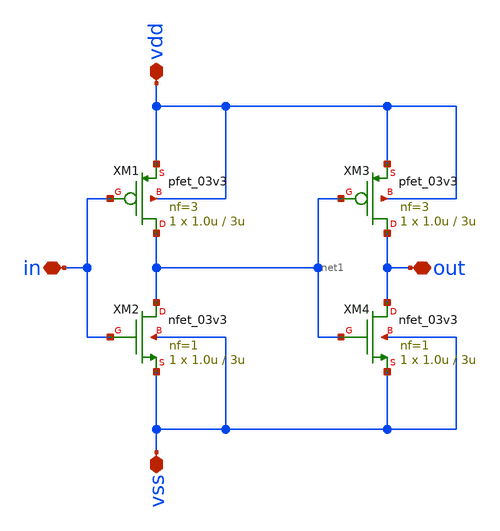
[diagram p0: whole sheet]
** sch_path: designs/libs/core_analog/asc_delay_1ns/asc_delay_1ns.sch
**.subckt asc_delay_1ns in vss vdd out
*.iopin in
*.iopin vss
*.iopin vdd
*.iopin out
XM1 net1 in vdd vdd pfet_03v3 L=3u W=1.0u nf=3 ad='int((nf+1)/2) * W/nf * 0.18u' as='int((nf+2)/2) * W/nf * 0.18u'
+ pd='2*int((nf+1)/2) * (W/nf + 0.18u)' ps='2*int((nf+2)/2) * (W/nf + 0.18u)' nrd='0.18u / W' nrs='0.18u / W'
+ sa=0 sb=0 sd=0 m=1
XM2 net1 in vss vss nfet_03v3 L=3u W=1.0u nf=1 ad='int((nf+1)/2) * W/nf * 0.18u' as='int((nf+2)/2) * W/nf * 0.18u'
+ pd='2*int((nf+1)/2) * (W/nf + 0.18u)' ps='2*int((nf+2)/2) * (W/nf + 0.18u)' nrd='0.18u / W' nrs='0.18u / W'
+ sa=0 sb=0 sd=0 m=1
XM3 out net1 vdd vdd pfet_03v3 L=3u W=1.0u nf=3 ad='int((nf+1)/2) * W/nf * 0.18u' as='int((nf+2)/2) * W/nf * 0.18u'
+ pd='2*int((nf+1)/2) * (W/nf + 0.18u)' ps='2*int((nf+2)/2) * (W/nf + 0.18u)' nrd='0.18u / W' nrs='0.18u / W'
+ sa=0 sb=0 sd=0 m=1
XM4 out net1 vss vss nfet_03v3 L=3u W=1.0u nf=1 ad='int((nf+1)/2) * W/nf * 0.18u' as='int((nf+2)/2) * W/nf * 0.18u'
+ pd='2*int((nf+1)/2) * (W/nf + 0.18u)' ps='2*int((nf+2)/2) * (W/nf + 0.18u)' nrd='0.18u / W' nrs='0.18u / W'
+ sa=0 sb=0 sd=0 m=1
**.ends
.end
